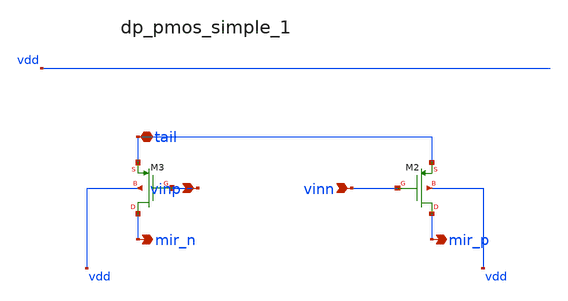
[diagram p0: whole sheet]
** sch_path: analog-db/raw/amp_025_hsu_classab_ota/hier/blocks/dp_pmos_simple_1.sch
**.subckt dp_pmos_simple_1 vinp vinn tail mir_n mir_p
*.ipin vinp
*.ipin vinn
*.iopin tail
*.opin mir_n
*.opin mir_p
XM2 mir_p vinn tail vdd sg13_lv_pmos w=x_dut_xm2_w l=x_dut_xm2_l ng=1 m=x_dut_xm2_m
XM3 mir_n vinp tail vdd sg13_lv_pmos w=x_dut_xm3_w l=x_dut_xm3_l ng=1 m=x_dut_xm3_m
**.ends
.end
